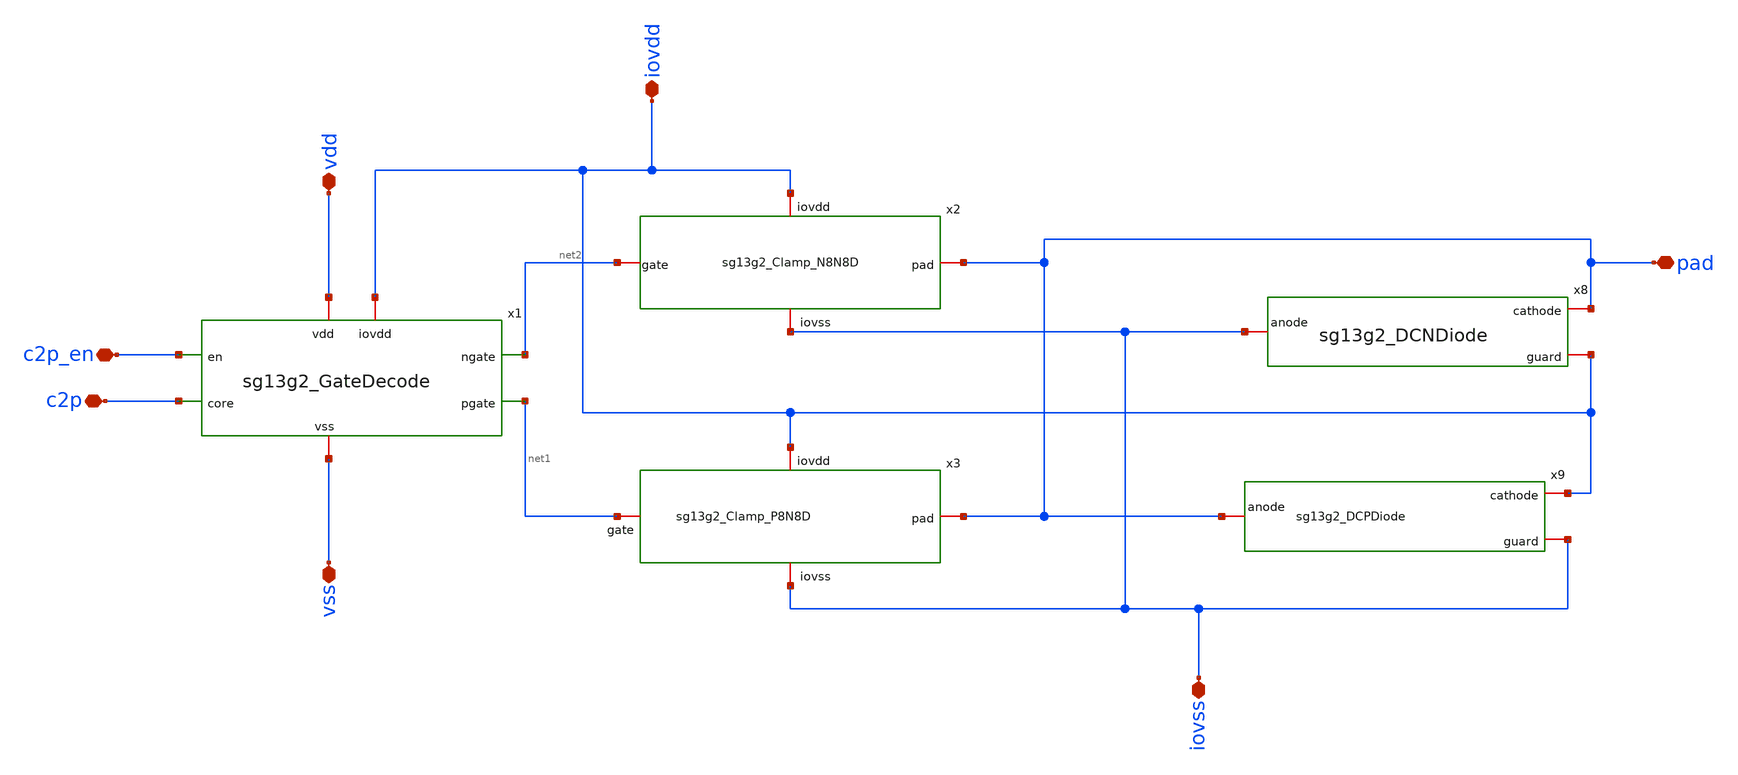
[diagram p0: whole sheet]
** sch_path: CDR4176-main/schematic/xschem/project_io/sg13g2_IOPadTriOut16mA/sg13g2_IOPadTriOut16mA.sch
**.subckt sg13g2_IOPadTriOut16mA iovss pad vss c2p vdd iovdd c2p_en
*.iopin iovss
*.iopin pad
*.iopin vss
*.iopin c2p
*.iopin vdd
*.iopin iovdd
*.iopin c2p_en
x8 pad iovss iovdd sg13g2_DCNDiode
x9 iovdd pad iovss sg13g2_DCPDiode
x1 vdd iovdd c2p_en net2 net1 c2p vss sg13g2_GateDecode
x2 iovdd pad net2 iovss sg13g2_Clamp_N8N8D
x3 iovdd net1 pad iovss sg13g2_Clamp_P8N8D
**.ends
.end
